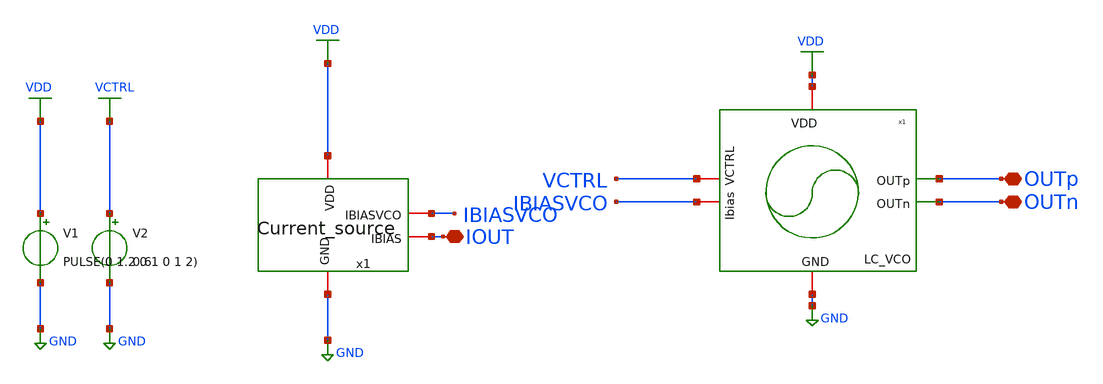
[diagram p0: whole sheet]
** sch_path: schematic/lc-vco/LC_VCO_cs_tb.sch
**.subckt LC_VCO_cs_tb OUTp OUTn IOUT
*.iopin OUTp
*.iopin OUTn
*.iopin IOUT
V2 VCTRL GND 0.6
x2 VDD OUTp OUTn IBIASVCO VCTRL GND LC_VCO
x1 IBIASVCO IOUT VDD GND Current_source
V1 VDD GND PULSE(0 1.2 0 1 0 1 2)
**** begin user architecture code



.include ./IHP_4nH_Inductor.spice
.param temp = 27

.control

* Initial condition
.ic v(OUTp)=0.6

* Simulation accuracy
.options reltol=1e-4 abstol=1e-9 maxstep=5p method=gear

* Save required signals
save time v(OUTp) v(CTRL)

* Long transient for ~10 kHz FFT resolution
tran 0.01n 0.5u UIC

* Save raw waveform
write LC_VCO_tb.raw

* Plot steady-state waveform
plot v(OUTp) xlimit 5n 60n

* FFT analysis
linearize v(OUTp)
fft v(OUTp)

let vmag = db(mag(v(OUTp)))

* Plot FFT spectrum
plot vmag vs frequency xlimit 0 5G

* Save FFT data
wrdata fft_output.txt frequency vmag

* Save waveform for external processing
wrdata vco_waveform.txt time v(OUTp)

.endc



 .lib cornerMOSlv.lib mos_tt
.lib cornerRES.lib res_typ
.lib $::SG13G2_MODELS/cornerCAP.lib cap_typ_stat

**** end user architecture code
**.ends
.GLOBAL GND
.GLOBAL VDD
.GLOBAL VCTRL
.end
